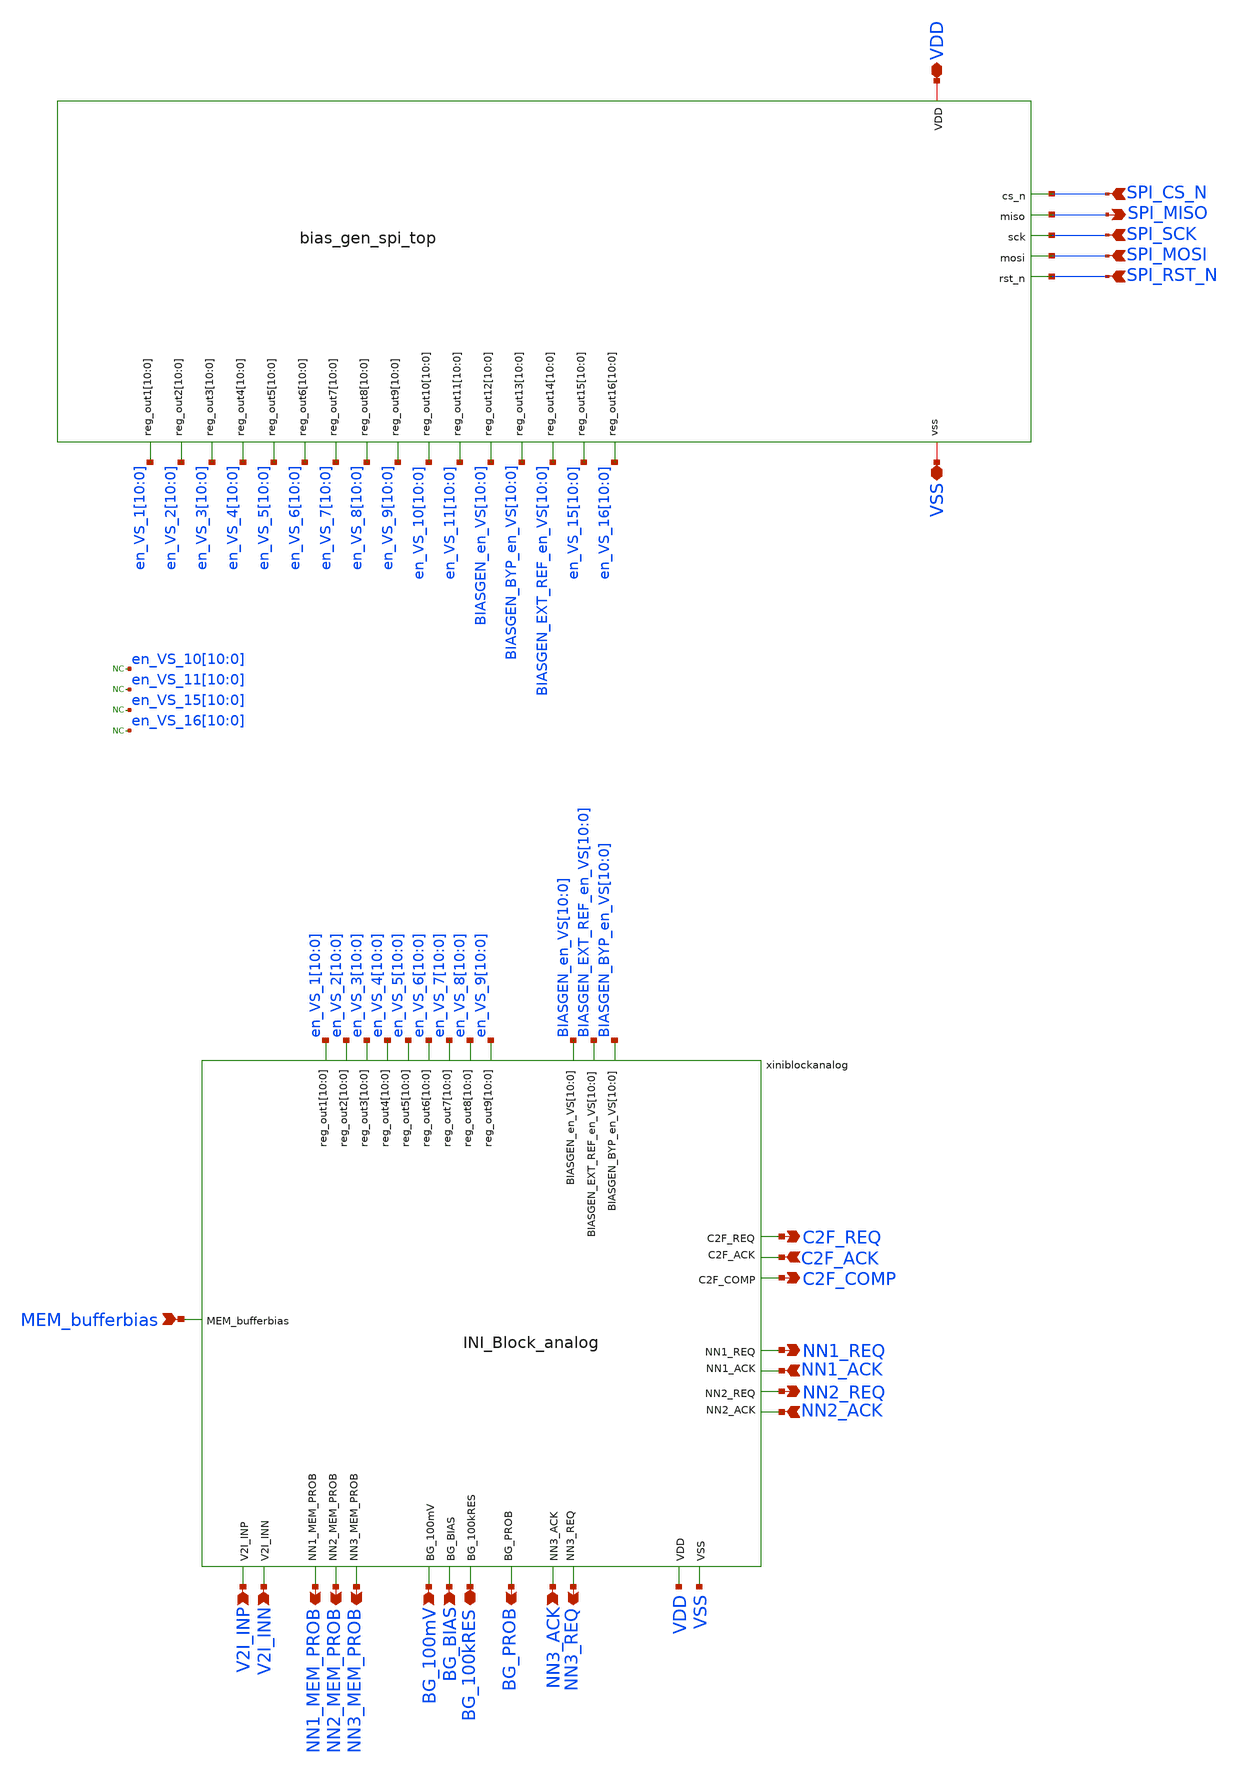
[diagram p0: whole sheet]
** sch_path: INI_Block.sch
**.subckt INI_Block SPI_CS_N SPI_MISO SPI_SCK SPI_MOSI SPI_RST_N VSS VDD MEM_bufferbias C2F_REQ
*+ C2F_COMP C2F_ACK NN1_REQ NN2_REQ NN3_REQ NN1_ACK NN2_ACK NN3_ACK V2I_INN V2I_INP NN1_MEM_PROB NN2_MEM_PROB
*+ NN3_MEM_PROB BG_100mV BG_BIAS BG_100kRES BG_PROB
*.ipin SPI_CS_N
*.opin SPI_MISO
*.ipin SPI_SCK
*.ipin SPI_MOSI
*.ipin SPI_RST_N
*.iopin VSS
*.iopin VDD
*.ipin MEM_bufferbias
*.opin C2F_REQ
*.opin C2F_COMP
*.ipin C2F_ACK
*.opin NN1_REQ
*.opin NN2_REQ
*.opin NN3_REQ
*.ipin NN1_ACK
*.ipin NN2_ACK
*.ipin NN3_ACK
*.ipin V2I_INN
*.ipin V2I_INP
*.opin NN1_MEM_PROB
*.opin NN2_MEM_PROB
*.opin NN3_MEM_PROB
*.ipin BG_100mV
*.ipin BG_BIAS
*.iopin BG_100kRES
*.opin BG_PROB
xspi SPI_CS_N SPI_MISO SPI_MOSI en_VS_10[0] en_VS_10[10] en_VS_10[1] en_VS_10[2] en_VS_10[3]
+ en_VS_10[4] en_VS_10[5] en_VS_10[6] en_VS_10[7] en_VS_10[8] en_VS_10[9] en_VS_11[0] en_VS_11[10] en_VS_11[1]
+ en_VS_11[2] en_VS_11[3] en_VS_11[4] en_VS_11[5] en_VS_11[6] en_VS_11[7] en_VS_11[8] en_VS_11[9]
+ BIASGEN_en_VS[0] BIASGEN_en_VS[10] BIASGEN_en_VS[1] BIASGEN_en_VS[2] BIASGEN_en_VS[3] BIASGEN_en_VS[4]
+ BIASGEN_en_VS[5] BIASGEN_en_VS[6] BIASGEN_en_VS[7] BIASGEN_en_VS[8] BIASGEN_en_VS[9] BIASGEN_BYP_en_VS[0]
+ BIASGEN_BYP_en_VS[10] BIASGEN_BYP_en_VS[1] BIASGEN_BYP_en_VS[2] BIASGEN_BYP_en_VS[3] BIASGEN_BYP_en_VS[4]
+ BIASGEN_BYP_en_VS[5] BIASGEN_BYP_en_VS[6] BIASGEN_BYP_en_VS[7] BIASGEN_BYP_en_VS[8] BIASGEN_BYP_en_VS[9]
+ BIASGEN_EXT_REF_en_VS[0] BIASGEN_EXT_REF_en_VS[10] BIASGEN_EXT_REF_en_VS[1] BIASGEN_EXT_REF_en_VS[2]
+ BIASGEN_EXT_REF_en_VS[3] BIASGEN_EXT_REF_en_VS[4] BIASGEN_EXT_REF_en_VS[5] BIASGEN_EXT_REF_en_VS[6] BIASGEN_EXT_REF_en_VS[7]
+ BIASGEN_EXT_REF_en_VS[8] BIASGEN_EXT_REF_en_VS[9] en_VS_15[0] en_VS_15[10] en_VS_15[1] en_VS_15[2] en_VS_15[3] en_VS_15[4]
+ en_VS_15[5] en_VS_15[6] en_VS_15[7] en_VS_15[8] en_VS_15[9] en_VS_16[0] en_VS_16[10] en_VS_16[1] en_VS_16[2]
+ en_VS_16[3] en_VS_16[4] en_VS_16[5] en_VS_16[6] en_VS_16[7] en_VS_16[8] en_VS_16[9] en_VS_1[0] en_VS_1[10]
+ en_VS_1[1] en_VS_1[2] en_VS_1[3] en_VS_1[4] en_VS_1[5] en_VS_1[6] en_VS_1[7] en_VS_1[8] en_VS_1[9] en_VS_2[0]
+ en_VS_2[10] en_VS_2[1] en_VS_2[2] en_VS_2[3] en_VS_2[4] en_VS_2[5] en_VS_2[6] en_VS_2[7] en_VS_2[8] en_VS_2[9]
+ en_VS_3[0] en_VS_3[10] en_VS_3[1] en_VS_3[2] en_VS_3[3] en_VS_3[4] en_VS_3[5] en_VS_3[6] en_VS_3[7] en_VS_3[8]
+ en_VS_3[9] en_VS_4[0] en_VS_4[10] en_VS_4[1] en_VS_4[2] en_VS_4[3] en_VS_4[4] en_VS_4[5] en_VS_4[6] en_VS_4[7]
+ en_VS_4[8] en_VS_4[9] en_VS_5[0] en_VS_5[10] en_VS_5[1] en_VS_5[2] en_VS_5[3] en_VS_5[4] en_VS_5[5] en_VS_5[6]
+ en_VS_5[7] en_VS_5[8] en_VS_5[9] en_VS_6[0] en_VS_6[10] en_VS_6[1] en_VS_6[2] en_VS_6[3] en_VS_6[4] en_VS_6[5]
+ en_VS_6[6] en_VS_6[7] en_VS_6[8] en_VS_6[9] en_VS_7[0] en_VS_7[10] en_VS_7[1] en_VS_7[2] en_VS_7[3] en_VS_7[4]
+ en_VS_7[5] en_VS_7[6] en_VS_7[7] en_VS_7[8] en_VS_7[9] en_VS_8[0] en_VS_8[10] en_VS_8[1] en_VS_8[2] en_VS_8[3]
+ en_VS_8[4] en_VS_8[5] en_VS_8[6] en_VS_8[7] en_VS_8[8] en_VS_8[9] en_VS_9[0] en_VS_9[10] en_VS_9[1] en_VS_9[2]
+ en_VS_9[3] en_VS_9[4] en_VS_9[5] en_VS_9[6] en_VS_9[7] en_VS_9[8] en_VS_9[9] SPI_RST_N SPI_SCK VDD VSS
+ bias_gen_spi_top
* noconn en_VS_11[10:0]
* noconn en_VS_10[10:0]
xiniblockanalog BIASGEN_en_VS[10] BIASGEN_en_VS[9] BIASGEN_en_VS[8] BIASGEN_en_VS[7]
+ BIASGEN_en_VS[6] BIASGEN_en_VS[5] BIASGEN_en_VS[4] BIASGEN_en_VS[3] BIASGEN_en_VS[2] BIASGEN_en_VS[1]
+ BIASGEN_en_VS[0] BIASGEN_BYP_en_VS[10] BIASGEN_BYP_en_VS[9] BIASGEN_BYP_en_VS[8] BIASGEN_BYP_en_VS[7]
+ BIASGEN_BYP_en_VS[6] BIASGEN_BYP_en_VS[5] BIASGEN_BYP_en_VS[4] BIASGEN_BYP_en_VS[3] BIASGEN_BYP_en_VS[2]
+ BIASGEN_BYP_en_VS[1] BIASGEN_BYP_en_VS[0] BIASGEN_EXT_REF_en_VS[10] BIASGEN_EXT_REF_en_VS[9] BIASGEN_EXT_REF_en_VS[8]
+ BIASGEN_EXT_REF_en_VS[7] BIASGEN_EXT_REF_en_VS[6] BIASGEN_EXT_REF_en_VS[5] BIASGEN_EXT_REF_en_VS[4] BIASGEN_EXT_REF_en_VS[3]
+ BIASGEN_EXT_REF_en_VS[2] BIASGEN_EXT_REF_en_VS[1] BIASGEN_EXT_REF_en_VS[0] en_VS_7[10] en_VS_7[9] en_VS_7[8] en_VS_7[7]
+ en_VS_7[6] en_VS_7[5] en_VS_7[4] en_VS_7[3] en_VS_7[2] en_VS_7[1] en_VS_7[0] en_VS_9[10] en_VS_9[9] en_VS_9[8]
+ en_VS_9[7] en_VS_9[6] en_VS_9[5] en_VS_9[4] en_VS_9[3] en_VS_9[2] en_VS_9[1] en_VS_9[0] en_VS_1[10] en_VS_1[9]
+ en_VS_1[8] en_VS_1[7] en_VS_1[6] en_VS_1[5] en_VS_1[4] en_VS_1[3] en_VS_1[2] en_VS_1[1] en_VS_1[0] en_VS_6[10]
+ en_VS_6[9] en_VS_6[8] en_VS_6[7] en_VS_6[6] en_VS_6[5] en_VS_6[4] en_VS_6[3] en_VS_6[2] en_VS_6[1] en_VS_6[0]
+ en_VS_5[10] en_VS_5[9] en_VS_5[8] en_VS_5[7] en_VS_5[6] en_VS_5[5] en_VS_5[4] en_VS_5[3] en_VS_5[2] en_VS_5[1]
+ en_VS_5[0] en_VS_3[10] en_VS_3[9] en_VS_3[8] en_VS_3[7] en_VS_3[6] en_VS_3[5] en_VS_3[4] en_VS_3[3] en_VS_3[2]
+ en_VS_3[1] en_VS_3[0] en_VS_8[10] en_VS_8[9] en_VS_8[8] en_VS_8[7] en_VS_8[6] en_VS_8[5] en_VS_8[4] en_VS_8[3]
+ en_VS_8[2] en_VS_8[1] en_VS_8[0] en_VS_2[10] en_VS_2[9] en_VS_2[8] en_VS_2[7] en_VS_2[6] en_VS_2[5] en_VS_2[4]
+ en_VS_2[3] en_VS_2[2] en_VS_2[1] en_VS_2[0] en_VS_4[10] en_VS_4[9] en_VS_4[8] en_VS_4[7] en_VS_4[6] en_VS_4[5]
+ en_VS_4[4] en_VS_4[3] en_VS_4[2] en_VS_4[1] en_VS_4[0] BG_PROB NN3_MEM_PROB NN3_REQ NN3_ACK NN2_MEM_PROB
+ NN2_REQ NN2_ACK VDD NN1_MEM_PROB V2I_INP NN1_REQ V2I_INN BG_100kRES NN1_ACK VSS BG_BIAS BG_100mV C2F_REQ
+ C2F_ACK C2F_COMP MEM_bufferbias INI_Block_analog
* noconn en_VS_16[10:0]
* noconn en_VS_15[10:0]
**.ends
.end
